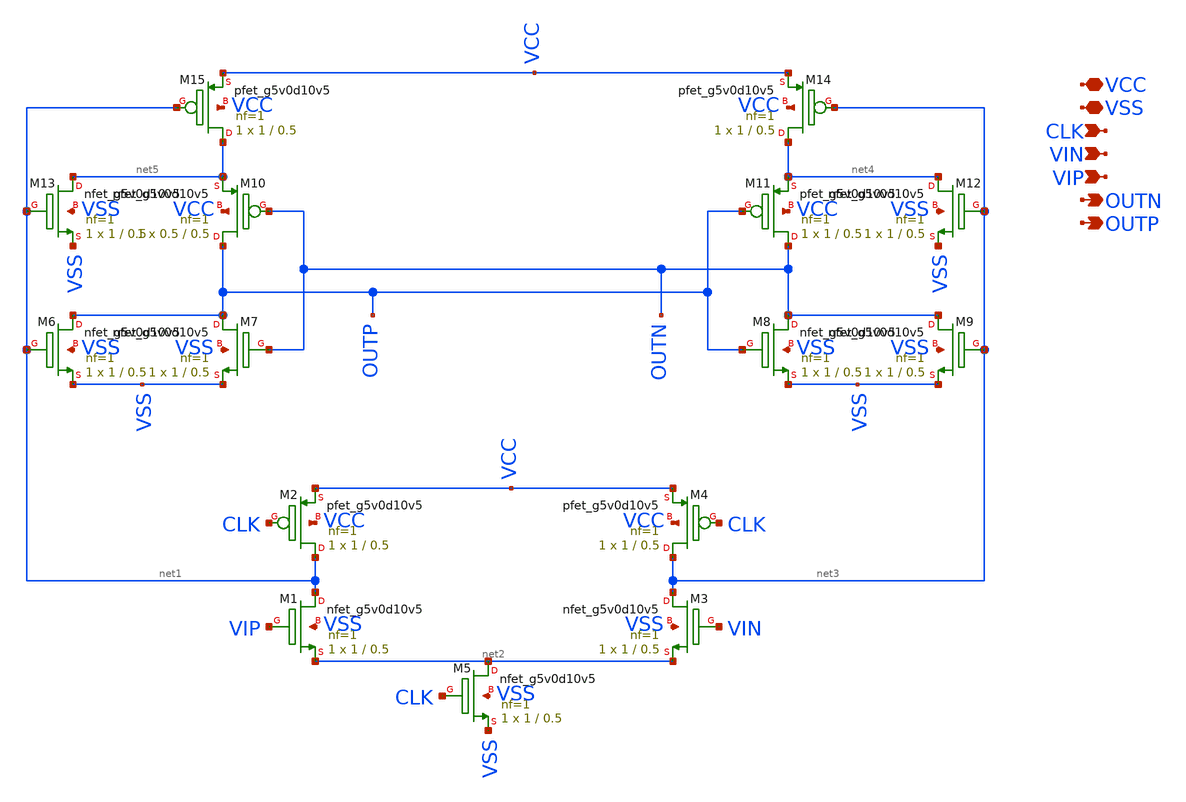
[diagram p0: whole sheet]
** sch_path: Comparator/schematic/miyahara_comparator.sch
**.subckt miyahara_comparator VCC CLK OUTN OUTP VIN VIP VSS
*.iopin VCC
*.ipin CLK
*.opin OUTN
*.opin OUTP
*.ipin VIN
*.ipin VIP
*.iopin VSS
XM1 net1 VIP net2 VSS sky130_fd_pr__nfet_g5v0d10v5 L=0.5 W=1 nf=1 ad='int((nf+1)/2) * W/nf * 0.29' as='int((nf+2)/2) * W/nf * 0.29'
+ pd='2*int((nf+1)/2) * (W/nf + 0.29)' ps='2*int((nf+2)/2) * (W/nf + 0.29)' nrd='0.29 / W' nrs='0.29 / W'
+ sa=0 sb=0 sd=0 mult=1 m=1
XM2 net1 CLK VCC VCC sky130_fd_pr__pfet_g5v0d10v5 L=0.5 W=1 nf=1 ad='int((nf+1)/2) * W/nf * 0.29' as='int((nf+2)/2) * W/nf * 0.29'
+ pd='2*int((nf+1)/2) * (W/nf + 0.29)' ps='2*int((nf+2)/2) * (W/nf + 0.29)' nrd='0.29 / W' nrs='0.29 / W'
+ sa=0 sb=0 sd=0 mult=1 m=1
XM3 net3 VIN net2 VSS sky130_fd_pr__nfet_g5v0d10v5 L=0.5 W=1 nf=1 ad='int((nf+1)/2) * W/nf * 0.29' as='int((nf+2)/2) * W/nf * 0.29'
+ pd='2*int((nf+1)/2) * (W/nf + 0.29)' ps='2*int((nf+2)/2) * (W/nf + 0.29)' nrd='0.29 / W' nrs='0.29 / W'
+ sa=0 sb=0 sd=0 mult=1 m=1
XM4 net3 CLK VCC VCC sky130_fd_pr__pfet_g5v0d10v5 L=0.5 W=1 nf=1 ad='int((nf+1)/2) * W/nf * 0.29' as='int((nf+2)/2) * W/nf * 0.29'
+ pd='2*int((nf+1)/2) * (W/nf + 0.29)' ps='2*int((nf+2)/2) * (W/nf + 0.29)' nrd='0.29 / W' nrs='0.29 / W'
+ sa=0 sb=0 sd=0 mult=1 m=1
XM5 net2 CLK VSS VSS sky130_fd_pr__nfet_g5v0d10v5 L=0.5 W=1 nf=1 ad='int((nf+1)/2) * W/nf * 0.29' as='int((nf+2)/2) * W/nf * 0.29'
+ pd='2*int((nf+1)/2) * (W/nf + 0.29)' ps='2*int((nf+2)/2) * (W/nf + 0.29)' nrd='0.29 / W' nrs='0.29 / W'
+ sa=0 sb=0 sd=0 mult=1 m=1
XM6 OUTP net1 VSS VSS sky130_fd_pr__nfet_g5v0d10v5 L=0.5 W=1 nf=1 ad='int((nf+1)/2) * W/nf * 0.29' as='int((nf+2)/2) * W/nf * 0.29'
+ pd='2*int((nf+1)/2) * (W/nf + 0.29)' ps='2*int((nf+2)/2) * (W/nf + 0.29)' nrd='0.29 / W' nrs='0.29 / W'
+ sa=0 sb=0 sd=0 mult=1 m=1
XM7 OUTP OUTN VSS VSS sky130_fd_pr__nfet_g5v0d10v5 L=0.5 W=1 nf=1 ad='int((nf+1)/2) * W/nf * 0.29' as='int((nf+2)/2) * W/nf * 0.29'
+ pd='2*int((nf+1)/2) * (W/nf + 0.29)' ps='2*int((nf+2)/2) * (W/nf + 0.29)' nrd='0.29 / W' nrs='0.29 / W'
+ sa=0 sb=0 sd=0 mult=1 m=1
XM8 OUTN OUTP VSS VSS sky130_fd_pr__nfet_g5v0d10v5 L=0.5 W=1 nf=1 ad='int((nf+1)/2) * W/nf * 0.29' as='int((nf+2)/2) * W/nf * 0.29'
+ pd='2*int((nf+1)/2) * (W/nf + 0.29)' ps='2*int((nf+2)/2) * (W/nf + 0.29)' nrd='0.29 / W' nrs='0.29 / W'
+ sa=0 sb=0 sd=0 mult=1 m=1
XM9 OUTN net3 VSS VSS sky130_fd_pr__nfet_g5v0d10v5 L=0.5 W=1 nf=1 ad='int((nf+1)/2) * W/nf * 0.29' as='int((nf+2)/2) * W/nf * 0.29'
+ pd='2*int((nf+1)/2) * (W/nf + 0.29)' ps='2*int((nf+2)/2) * (W/nf + 0.29)' nrd='0.29 / W' nrs='0.29 / W'
+ sa=0 sb=0 sd=0 mult=1 m=1
XM10 OUTP OUTN net5 VCC sky130_fd_pr__pfet_g5v0d10v5 L=0.5 W=0.5 nf=1 ad='int((nf+1)/2) * W/nf * 0.29'
+ as='int((nf+2)/2) * W/nf * 0.29' pd='2*int((nf+1)/2) * (W/nf + 0.29)' ps='2*int((nf+2)/2) * (W/nf + 0.29)'
+ nrd='0.29 / W' nrs='0.29 / W' sa=0 sb=0 sd=0 mult=1 m=1
XM11 OUTN OUTP net4 VCC sky130_fd_pr__pfet_g5v0d10v5 L=0.5 W=1 nf=1 ad='int((nf+1)/2) * W/nf * 0.29'
+ as='int((nf+2)/2) * W/nf * 0.29' pd='2*int((nf+1)/2) * (W/nf + 0.29)' ps='2*int((nf+2)/2) * (W/nf + 0.29)'
+ nrd='0.29 / W' nrs='0.29 / W' sa=0 sb=0 sd=0 mult=1 m=1
XM12 net4 net3 VSS VSS sky130_fd_pr__nfet_g5v0d10v5 L=0.5 W=1 nf=1 ad='int((nf+1)/2) * W/nf * 0.29' as='int((nf+2)/2) * W/nf * 0.29'
+ pd='2*int((nf+1)/2) * (W/nf + 0.29)' ps='2*int((nf+2)/2) * (W/nf + 0.29)' nrd='0.29 / W' nrs='0.29 / W'
+ sa=0 sb=0 sd=0 mult=1 m=1
XM13 net5 net1 VSS VSS sky130_fd_pr__nfet_g5v0d10v5 L=0.5 W=1 nf=1 ad='int((nf+1)/2) * W/nf * 0.29' as='int((nf+2)/2) * W/nf * 0.29'
+ pd='2*int((nf+1)/2) * (W/nf + 0.29)' ps='2*int((nf+2)/2) * (W/nf + 0.29)' nrd='0.29 / W' nrs='0.29 / W'
+ sa=0 sb=0 sd=0 mult=1 m=1
XM14 net4 net3 VCC VCC sky130_fd_pr__pfet_g5v0d10v5 L=0.5 W=1 nf=1 ad='int((nf+1)/2) * W/nf * 0.29' as='int((nf+2)/2) * W/nf * 0.29'
+ pd='2*int((nf+1)/2) * (W/nf + 0.29)' ps='2*int((nf+2)/2) * (W/nf + 0.29)' nrd='0.29 / W' nrs='0.29 / W'
+ sa=0 sb=0 sd=0 mult=1 m=1
XM15 net5 net1 VCC VCC sky130_fd_pr__pfet_g5v0d10v5 L=0.5 W=1 nf=1 ad='int((nf+1)/2) * W/nf * 0.29' as='int((nf+2)/2) * W/nf * 0.29'
+ pd='2*int((nf+1)/2) * (W/nf + 0.29)' ps='2*int((nf+2)/2) * (W/nf + 0.29)' nrd='0.29 / W' nrs='0.29 / W'
+ sa=0 sb=0 sd=0 mult=1 m=1
**.ends
.end
